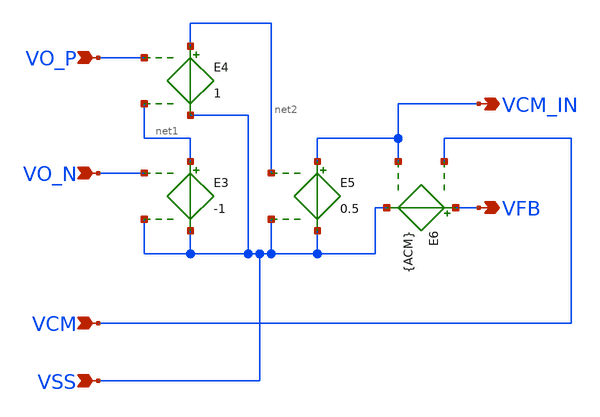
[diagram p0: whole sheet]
** sch_path: circuit-level/xschem/frontend/frontend_cmfb_ideal.sch
**.subckt frontend_cmfb_ideal VO_P VO_N VCM VSS VFB VCM_IN
*.ipin VO_P
*.ipin VO_N
*.ipin VCM
*.ipin VSS
*.opin VFB
*.opin VCM_IN
E3 net1 VSS VO_N VSS -1
E4 net2 VSS VO_P net1 1
E5 VCM_IN VSS net2 VSS 0.5
E6 VFB VSS VCM VCM_IN {ACM}
**.ends
.end
